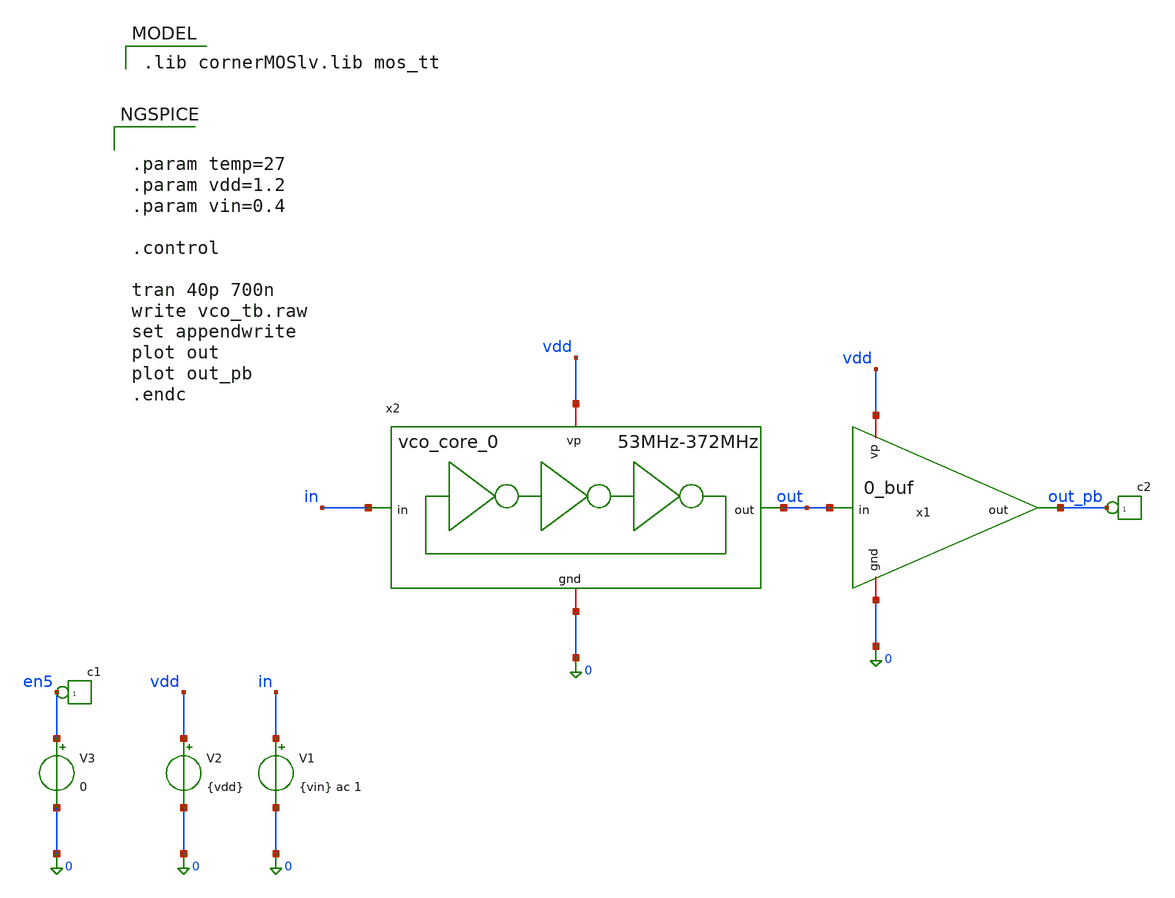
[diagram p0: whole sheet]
** sch_path: schematics/vco/vco_tb/vco_dcin_tb.sch
**.subckt vco_dcin_tb
V1 in 0 {vin} ac 1
.save i(v1)
V2 vdd 0 {vdd}
*connector(1,1) ?1 out_pb
x2 vdd 0 out in vco_core_0
V3 en5 0 0
*connector(1,1) ?1 en5
x1 vdd 0 out_pb out 0_buf
**** begin user architecture code


.param temp=27
.param vdd=1.2
.param vin=0.4

.control

tran 40p 700n
write vco_tb.raw
set appendwrite
plot out
plot out_pb
.endc


 .lib cornerMOSlv.lib mos_tt

**** end user architecture code
**.ends

* expanding   symbol:  /foss/designs/CHIP-PLL/schematics/vco/vco_cell/vco_core_0.sym # of pins=4
** sym_path: schematics/vco/vco_cell/vco_core_0.sym
** sch_path: schematics/vco/vco_cell/vco_core_0.sch
.subckt vco_core_0 vp gnd out in
*.ipin in
*.iopin vp
*.opin out
*.iopin gnd
XM1 pgt in gnd gnd sg13_lv_nmos w=0.8u l=0.14*4u ng=1 m=1 mm_ok=1
XM2 pgt pgt vp vp sg13_lv_pmos w=1.2u l=0.14*4u ng=1 m=1 mm_ok=1
x1 vp pgt out net1 in gnd vco_delay_cell_0
x2 vp pgt net1 2th in gnd vco_delay_cell_0
x3 vp pgt 2th 3th in gnd vco_delay_cell_0
x4 vp pgt 3th 4th in gnd vco_delay_cell_0
x7 vp pgt 4th out in gnd vco_delay_cell_0
.ends


* expanding   symbol:  /foss/designs/CHIP-PLL/schematics/vco/vco_cell/0_buf.sym # of pins=4
** sym_path: schematics/vco/vco_cell/0_buf.sym
** sch_path: schematics/vco/vco_cell/0_buf.sch
.subckt 0_buf vp gnd out in
*.ipin in
*.opin out
*.iopin vp
*.iopin gnd
XM24 1_stg in vp vp sg13_lv_pmos w=1.2u l=0.16*2u ng=1 m=1 mm_ok=1
XM25 1_stg in gnd gnd sg13_lv_nmos w=0.8u l=0.16*2u ng=1 m=1 mm_ok=1
XM1 2_stg 1_stg vp vp sg13_lv_pmos w=1.5*1.2u l=0.16*2u ng=1 m=1 mm_ok=1
XM2 2_stg 1_stg gnd gnd sg13_lv_nmos w=1.5*1u l=0.16*2u ng=1 m=1 mm_ok=1
XM3 3_stg 2_stg vp vp sg13_lv_pmos w=2*1.2u l=0.16*2u ng=1 m=1 mm_ok=1
XM4 3_stg 2_stg gnd gnd sg13_lv_nmos w=2*1u l=0.16*2u ng=1 m=1 mm_ok=1
XM5 out 3_stg vp vp sg13_lv_pmos w=2*1.2u l=0.16*2u ng=1 m=1 mm_ok=1
XM6 out 3_stg gnd gnd sg13_lv_nmos w=2*1u l=0.16*2u ng=1 m=1 mm_ok=1
.ends


* expanding   symbol:  /foss/designs/CHIP-PLL/schematics/vco/vco_cell/vco_delay_cell_0.sym # of
*+ pins=6
** sym_path: schematics/vco/vco_cell/vco_delay_cell_0.sym
** sch_path: schematics/vco/vco_cell/vco_delay_cell_0.sch
.subckt vco_delay_cell_0 vp pgt in out ngt gnd
*.ipin in
*.opin out
*.iopin gnd
*.iopin vp
*.iopin pgt
*.iopin ngt
XM23 up pgt vp vp sg13_lv_pmos w=1.2u l=0.14*4u ng=1 m=1 mm_ok=1
XM1 out in up vp sg13_lv_pmos w=1.2u l=0.14*2u ng=1 m=1 mm_ok=1
XM2 out in dn gnd sg13_lv_nmos w=0.8u l=0.14*2u ng=1 m=1 mm_ok=1
XM26 dn ngt gnd gnd sg13_lv_nmos w=0.8u l=0.14*4u ng=1 m=1 mm_ok=1
.ends

.end
